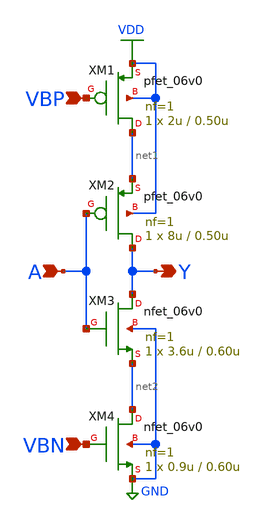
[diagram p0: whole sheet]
** sch_path: PLL/xschem/inv_bias.sch
**.subckt inv_bias Y A VBP VBN
*.opin Y
*.ipin A
*.ipin VBP
*.ipin VBN
XM1 net1 VBP VDD VDD pfet_06v0 L=0.50u W=2u nf=1 ad='int((nf+1)/2) * W/nf * 0.18u' as='int((nf+2)/2) * W/nf * 0.18u'
+ pd='2*int((nf+1)/2) * (W/nf + 0.18u)' ps='2*int((nf+2)/2) * (W/nf + 0.18u)' nrd='0.18u / W' nrs='0.18u / W'
+ sa=0 sb=0 sd=0 m=1
XM2 Y A net1 VDD pfet_06v0 L=0.50u W=8u nf=1 ad='int((nf+1)/2) * W/nf * 0.18u' as='int((nf+2)/2) * W/nf * 0.18u'
+ pd='2*int((nf+1)/2) * (W/nf + 0.18u)' ps='2*int((nf+2)/2) * (W/nf + 0.18u)' nrd='0.18u / W' nrs='0.18u / W'
+ sa=0 sb=0 sd=0 m=1
XM3 Y A net2 GND nfet_06v0 L=0.60u W=3.6u nf=1 ad='int((nf+1)/2) * W/nf * 0.18u' as='int((nf+2)/2) * W/nf * 0.18u'
+ pd='2*int((nf+1)/2) * (W/nf + 0.18u)' ps='2*int((nf+2)/2) * (W/nf + 0.18u)' nrd='0.18u / W' nrs='0.18u / W'
+ sa=0 sb=0 sd=0 m=1
XM4 net2 VBN GND GND nfet_06v0 L=0.60u W=0.9u nf=1 ad='int((nf+1)/2) * W/nf * 0.18u' as='int((nf+2)/2) * W/nf * 0.18u'
+ pd='2*int((nf+1)/2) * (W/nf + 0.18u)' ps='2*int((nf+2)/2) * (W/nf + 0.18u)' nrd='0.18u / W' nrs='0.18u / W'
+ sa=0 sb=0 sd=0 m=1
**.ends
.GLOBAL VDD
.GLOBAL GND
.end
